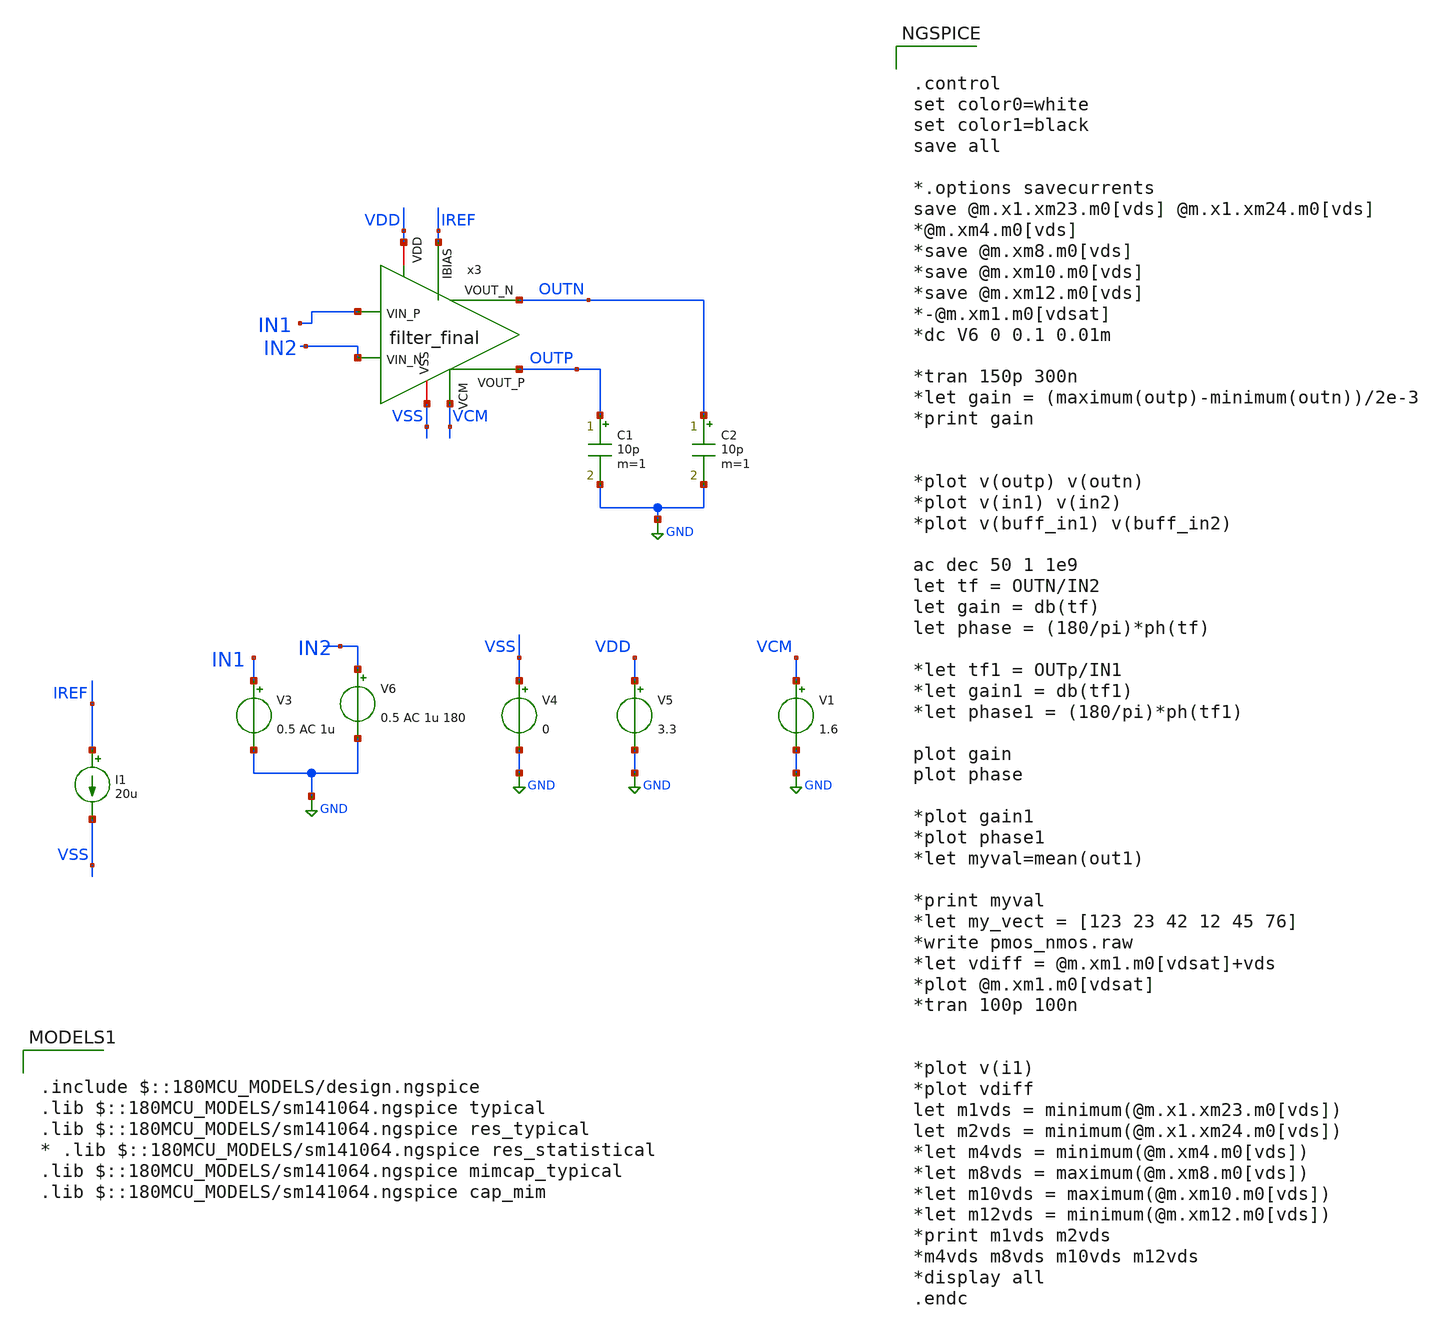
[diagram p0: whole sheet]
** sch_path: AWG_OUTPUT_AND_MUX_PAKISTAN_05/xschem/filter_test.sch
**.subckt filter_test
V3 IN1 GND 0.5 AC 1u
V4 VSS GND 0
V5 VDD GND 3.3
V6 IN2 GND 0.5 AC 1u 180
I1 IREF VSS 20u
C1 OUTP GND 10p m=1
C2 OUTN GND 10p m=1
V1 VCM GND 1.6
x3 IN2 IN1 OUTP OUTN VDD IREF VCM VSS filter_final
**** begin user architecture code


.control
set color0=white
set color1=black
save all

*.options savecurrents
save @m.x1.xm23.m0[vds] @m.x1.xm24.m0[vds]
*@m.xm4.m0[vds]
*save @m.xm8.m0[vds]
*save @m.xm10.m0[vds]
*save @m.xm12.m0[vds]
*-@m.xm1.m0[vdsat]
*dc V6 0 0.1 0.01m

*tran 150p 300n
*let gain = (maximum(outp)-minimum(outn))/2e-3
*print gain


*plot v(outp) v(outn)
*plot v(in1) v(in2)
*plot v(buff_in1) v(buff_in2)

ac dec 50 1 1e9
let tf = OUTN/IN2
let gain = db(tf)
let phase = (180/pi)*ph(tf)

*let tf1 = OUTp/IN1
*let gain1 = db(tf1)
*let phase1 = (180/pi)*ph(tf1)

plot gain
plot phase

*plot gain1
*plot phase1
*let myval=mean(out1)

*print myval
*let my_vect = [123 23 42 12 45 76]
*write pmos_nmos.raw
*let vdiff = @m.xm1.m0[vdsat]+vds
*plot @m.xm1.m0[vdsat]
*tran 100p 100n


*plot v(i1)
*plot vdiff
let m1vds = minimum(@m.x1.xm23.m0[vds])
let m2vds = minimum(@m.x1.xm24.m0[vds])
*let m4vds = minimum(@m.xm4.m0[vds])
*let m8vds = maximum(@m.xm8.m0[vds])
*let m10vds = maximum(@m.xm10.m0[vds])
*let m12vds = minimum(@m.xm12.m0[vds])
*print m1vds m2vds
*m4vds m8vds m10vds m12vds
*display all
.endc



.include $::180MCU_MODELS/design.ngspice
.lib $::180MCU_MODELS/sm141064.ngspice typical
.lib $::180MCU_MODELS/sm141064.ngspice res_typical
* .lib $::180MCU_MODELS/sm141064.ngspice res_statistical
.lib $::180MCU_MODELS/sm141064.ngspice mimcap_typical
.lib $::180MCU_MODELS/sm141064.ngspice cap_mim

**** end user architecture code
**.ends

* expanding   symbol:  filter_final.sym # of pins=8
** sym_path: AWG_OUTPUT_AND_MUX_PAKISTAN_05/xschem/filter_final.sym
** sch_path: AWG_OUTPUT_AND_MUX_PAKISTAN_05/xschem/filter_final.sch
.subckt filter_final VIN_N VIN_P VOUT_P VOUT_N VDD IBIAS VCM VSS
*.iopin VDD
*.iopin VSS
*.opin VOUT_N
*.opin VOUT_P
*.ipin VIN_N
*.ipin VIN_P
*.ipin IBIAS
*.ipin VCM
XR37 net7 VIN_P VDD ppolyf_u r_width=1e-6 r_length=2.3e-6 m=1
XR1 net1 VIN_N VDD ppolyf_u r_width=1e-6 r_length=2.3e-6 m=1
XR2 net8 net7 VDD ppolyf_u r_width=1e-6 r_length=2.3e-6 m=1
XR3 net2 net1 VDD ppolyf_u r_width=1e-6 r_length=2.3e-6 m=1
XR4 R7_R3_P net8 VDD ppolyf_u r_width=1e-6 r_length=2.3e-6 m=1
XR5 R7_R3_N net2 VDD ppolyf_u r_width=1e-6 r_length=2.3e-6 m=1
XR6 net9 R7_R3_P VDD ppolyf_u r_width=1e-6 r_length=2.3e-6 m=1
XR7 net3 R7_R3_N VDD ppolyf_u r_width=1e-6 r_length=2.3e-6 m=1
XR8 net10 net9 VDD ppolyf_u r_width=1e-6 r_length=2.3e-6 m=1
XR9 net4 net3 VDD ppolyf_u r_width=1e-6 r_length=2.3e-6 m=1
XR10 net12 net10 VDD ppolyf_u r_width=1e-6 r_length=2.3e-6 m=1
XR11 net50 net4 VDD ppolyf_u r_width=1e-6 r_length=2.3e-6 m=1
XR12 net11 net12 VDD ppolyf_u r_width=1e-6 r_length=2.3e-6 m=1
XR13 net5 net50 VDD ppolyf_u r_width=1e-6 r_length=2.3e-6 m=1
XR14 net13 net11 VDD ppolyf_u r_width=1e-6 r_length=2.3e-6 m=1
XR15 net6 net5 VDD ppolyf_u r_width=1e-6 r_length=2.3e-6 m=1
XR16 net14 net13 VDD ppolyf_u r_width=1e-6 r_length=2.3e-6 m=1
XR17 net15 net6 VDD ppolyf_u r_width=1e-6 r_length=2.3e-6 m=1
XR18 R7_R10_R8_P net14 VDD ppolyf_u r_width=1e-6 r_length=2.3e-6 m=1
XR19 R7_R10_R8_N net15 VDD ppolyf_u r_width=1e-6 r_length=2.3e-6 m=1
XR20 net20 R7_R10_R8_P VDD ppolyf_u r_width=1e-6 r_length=2.3e-6 m=1
XR21 net16 R7_R10_R8_N VDD ppolyf_u r_width=1e-6 r_length=2.3e-6 m=1
XR22 net21 net20 VDD ppolyf_u r_width=1e-6 r_length=2.3e-6 m=1
XR23 net17 net16 VDD ppolyf_u r_width=1e-6 r_length=2.3e-6 m=1
XR24 net23 net21 VDD ppolyf_u r_width=1e-6 r_length=2.3e-6 m=1
XR25 net49 net17 VDD ppolyf_u r_width=1e-6 r_length=2.3e-6 m=1
XR26 net22 net23 VDD ppolyf_u r_width=1e-6 r_length=2.3e-6 m=1
XR27 net18 net49 VDD ppolyf_u r_width=1e-6 r_length=2.3e-6 m=1
XR28 net24 net22 VDD ppolyf_u r_width=1e-6 r_length=2.3e-6 m=1
XR29 net19 net18 VDD ppolyf_u r_width=1e-6 r_length=2.3e-6 m=1
XR30 net25 net24 VDD ppolyf_u r_width=1e-6 r_length=2.3e-6 m=1
XR31 net26 net19 VDD ppolyf_u r_width=1e-6 r_length=2.3e-6 m=1
XR32 net27 net25 VDD ppolyf_u r_width=1e-6 r_length=2.3e-6 m=1
XR33 net28 net26 VDD ppolyf_u r_width=1e-6 r_length=2.3e-6 m=1
XR34 net46 net27 VDD ppolyf_u r_width=1e-6 r_length=2.3e-6 m=1
XR35 net47 net28 VDD ppolyf_u r_width=1e-6 r_length=2.3e-6 m=1
XR36 net29 R7_R10_R8_N VDD ppolyf_u r_width=1e-6 r_length=2.3e-6 m=1
XR38 net30 net29 VDD ppolyf_u r_width=1e-6 r_length=2.3e-6 m=1
XR39 net48 net30 VDD ppolyf_u r_width=1e-6 r_length=2.3e-6 m=1
XR40 net31 net48 VDD ppolyf_u r_width=1e-6 r_length=2.3e-6 m=1
XR41 net32 net31 VDD ppolyf_u r_width=1e-6 r_length=2.3e-6 m=1
XR42 net33 net32 VDD ppolyf_u r_width=1e-6 r_length=2.3e-6 m=1
XR43 net34 net33 VDD ppolyf_u r_width=1e-6 r_length=2.3e-6 m=1
XR44 net45 net34 VDD ppolyf_u r_width=1e-6 r_length=2.3e-6 m=1
XR45 net35 net42 VDD ppolyf_u r_width=1e-6 r_length=2.3e-6 m=1
XR46 net36 net35 VDD ppolyf_u r_width=1e-6 r_length=2.3e-6 m=1
XR47 net38 net36 VDD ppolyf_u r_width=1e-6 r_length=2.3e-6 m=1
XR48 net37 net38 VDD ppolyf_u r_width=1e-6 r_length=2.3e-6 m=1
XR49 net39 net37 VDD ppolyf_u r_width=1e-6 r_length=2.3e-6 m=1
XR50 net40 net39 VDD ppolyf_u r_width=1e-6 r_length=2.3e-6 m=1
XR51 net41 net40 VDD ppolyf_u r_width=1e-6 r_length=2.3e-6 m=1
XR52 R7_R10_R8_P net41 VDD ppolyf_u r_width=1e-6 r_length=2.3e-6 m=1
XR53 net43 VOUT_N VDD ppolyf_u r_width=1e-6 r_length=2.3e-6 m=1
XR54 net42 net43 VDD ppolyf_u r_width=1e-6 r_length=2.3e-6 m=1
XR55 net44 net45 VDD ppolyf_u r_width=1e-6 r_length=2.3e-6 m=1
XR56 VOUT_P net44 VDD ppolyf_u r_width=1e-6 r_length=2.3e-6 m=1
XR57 net46 net46 VDD ppolyf_u r_width=1e-6 r_length=2.3e-6 m=1
XR58 net47 net47 VDD ppolyf_u r_width=1e-6 r_length=2.3e-6 m=1
XR59 net46 net46 VDD ppolyf_u r_width=1e-6 r_length=2.3e-6 m=1
XR60 net47 net47 VDD ppolyf_u r_width=1e-6 r_length=2.3e-6 m=1
XC5 VOUT_N net46 cap_mim_2f0_m4m5_noshield c_width=16e-6 c_length=15.2e-6 m=1
XC6 VOUT_P net47 cap_mim_2f0_m4m5_noshield c_width=16e-6 c_length=15.2e-6 m=1
XR61 VDD VDD VDD ppolyf_u r_width=1e-6 r_length=2.3e-6 m=1
XR62 VDD VDD VDD ppolyf_u r_width=1e-6 r_length=2.3e-6 m=1
XR63 VDD VDD VDD ppolyf_u r_width=1e-6 r_length=2.3e-6 m=1
XR64 VDD VDD VDD ppolyf_u r_width=1e-6 r_length=2.3e-6 m=1
XR65 VDD VDD VDD ppolyf_u r_width=1e-6 r_length=2.3e-6 m=1
XR66 VDD VDD VDD ppolyf_u r_width=1e-6 r_length=2.3e-6 m=1
XR67 VDD VDD VDD ppolyf_u r_width=1e-6 r_length=2.3e-6 m=1
XR68 VDD VDD VDD ppolyf_u r_width=1e-6 r_length=2.3e-6 m=1
XR69 VDD VDD VDD ppolyf_u r_width=1e-6 r_length=2.3e-6 m=1
XR70 VDD VDD VDD ppolyf_u r_width=1e-6 r_length=2.3e-6 m=1
XR71 VDD VDD VDD ppolyf_u r_width=1e-6 r_length=2.3e-6 m=1
XR72 VDD VDD VDD ppolyf_u r_width=1e-6 r_length=2.3e-6 m=1
XC8 VOUT_P net47 cap_mim_2f0_m4m5_noshield c_width=16e-6 c_length=15.2e-6 m=1
XC9 VOUT_N net46 cap_mim_2f0_m4m5_noshield c_width=16e-6 c_length=15.2e-6 m=1
x1 VDD VSS net47 net46 IBIAS VCM VOUT_N VOUT_P Folded_Cascode_Diff
XC1 R7_R10_R8_N R7_R10_R8_P cap_mim_2f0_m4m5_noshield c_width=16e-6 c_length=15.2e-6 m=1
XC2 R7_R10_R8_N R7_R10_R8_P cap_mim_2f0_m4m5_noshield c_width=16e-6 c_length=15.2e-6 m=1
XC3 R7_R3_P R7_R3_N cap_mim_2f0_m4m5_noshield c_width=16e-6 c_length=15.2e-6 m=1
XC4 R7_R3_P R7_R3_N cap_mim_2f0_m4m5_noshield c_width=16e-6 c_length=15.2e-6 m=1
XC7 R7_R3_P R7_R3_N cap_mim_2f0_m4m5_noshield c_width=16e-6 c_length=15.2e-6 m=1
XC10 R7_R3_P R7_R3_N cap_mim_2f0_m4m5_noshield c_width=16e-6 c_length=15.2e-6 m=1
XC12 R7_R3_P R7_R3_N cap_mim_2f0_m4m5_noshield c_width=16e-6 c_length=15.2e-6 m=1
XC13 R7_R3_P R7_R3_N cap_mim_2f0_m4m5_noshield c_width=16e-6 c_length=15.2e-6 m=1
.ends


* expanding   symbol:  Folded_Cascode_Diff.sym # of pins=8
** sym_path: AWG_OUTPUT_AND_MUX_PAKISTAN_05/xschem/Folded_Cascode_Diff.sym
** sch_path: AWG_OUTPUT_AND_MUX_PAKISTAN_05/xschem/Folded_Cascode_Diff.sch
.subckt Folded_Cascode_Diff VDD VSS IN_N IN_P IBIAS1 VCM OUT_N OUT_P
*.iopin VDD
*.iopin VSS
*.iopin IN_N
*.iopin IN_P
*.iopin IBIAS1
*.iopin VCM
*.iopin OUT_N
*.iopin OUT_P
XM1 VPD VB1 VDD VDD pfet_03v3 L=0.28u W=50u nf=1 ad='int((nf+1)/2) * W/nf * 0.18u' as='int((nf+2)/2) * W/nf * 0.18u'
+ pd='2*int((nf+1)/2) * (W/nf + 0.18u)' ps='2*int((nf+2)/2) * (W/nf + 0.18u)' nrd='0.18u / W' nrs='0.18u / W'
+ sa=0 sb=0 sd=0 m=1
XM2 VND VB1 VDD VDD pfet_03v3 L=0.28u W=50u nf=1 ad='int((nf+1)/2) * W/nf * 0.18u' as='int((nf+2)/2) * W/nf * 0.18u'
+ pd='2*int((nf+1)/2) * (W/nf + 0.18u)' ps='2*int((nf+2)/2) * (W/nf + 0.18u)' nrd='0.18u / W' nrs='0.18u / W'
+ sa=0 sb=0 sd=0 m=1
XM3 OUT1 VB2 VND VDD pfet_03v3 L=0.28u W=50u nf=1 ad='int((nf+1)/2) * W/nf * 0.18u' as='int((nf+2)/2) * W/nf * 0.18u'
+ pd='2*int((nf+1)/2) * (W/nf + 0.18u)' ps='2*int((nf+2)/2) * (W/nf + 0.18u)' nrd='0.18u / W' nrs='0.18u / W'
+ sa=0 sb=0 sd=0 m=1
XM4 OUT2 VB2 VPD VDD pfet_03v3 L=0.28u W=50u nf=1 ad='int((nf+1)/2) * W/nf * 0.18u' as='int((nf+2)/2) * W/nf * 0.18u'
+ pd='2*int((nf+1)/2) * (W/nf + 0.18u)' ps='2*int((nf+2)/2) * (W/nf + 0.18u)' nrd='0.18u / W' nrs='0.18u / W'
+ sa=0 sb=0 sd=0 m=1
XM5 OUT2 VB3 IPD VSS nfet_03v3 L=0.28u W=46u nf=1 ad='int((nf+1)/2) * W/nf * 0.18u' as='int((nf+2)/2) * W/nf * 0.18u'
+ pd='2*int((nf+1)/2) * (W/nf + 0.18u)' ps='2*int((nf+2)/2) * (W/nf + 0.18u)' nrd='0.18u / W' nrs='0.18u / W'
+ sa=0 sb=0 sd=0 m=1
XM6 OUT1 VB3 IND VSS nfet_03v3 L=0.28u W=46u nf=1 ad='int((nf+1)/2) * W/nf * 0.18u' as='int((nf+2)/2) * W/nf * 0.18u'
+ pd='2*int((nf+1)/2) * (W/nf + 0.18u)' ps='2*int((nf+2)/2) * (W/nf + 0.18u)' nrd='0.18u / W' nrs='0.18u / W'
+ sa=0 sb=0 sd=0 m=1
XM7 IPD VB4 VSS VSS nfet_03v3 L=0.28u W=92u nf=1 ad='int((nf+1)/2) * W/nf * 0.18u' as='int((nf+2)/2) * W/nf * 0.18u'
+ pd='2*int((nf+1)/2) * (W/nf + 0.18u)' ps='2*int((nf+2)/2) * (W/nf + 0.18u)' nrd='0.18u / W' nrs='0.18u / W'
+ sa=0 sb=0 sd=0 m=1
XM8 IND VB4 VSS VSS nfet_03v3 L=0.28u W=92u nf=1 ad='int((nf+1)/2) * W/nf * 0.18u' as='int((nf+2)/2) * W/nf * 0.18u'
+ pd='2*int((nf+1)/2) * (W/nf + 0.18u)' ps='2*int((nf+2)/2) * (W/nf + 0.18u)' nrd='0.18u / W' nrs='0.18u / W'
+ sa=0 sb=0 sd=0 m=1
XM9 BD IBIAS VDD VDD pfet_03v3 L=0.56u W=100u nf=1 ad='int((nf+1)/2) * W/nf * 0.18u' as='int((nf+2)/2) * W/nf * 0.18u'
+ pd='2*int((nf+1)/2) * (W/nf + 0.18u)' ps='2*int((nf+2)/2) * (W/nf + 0.18u)' nrd='0.18u / W' nrs='0.18u / W'
+ sa=0 sb=0 sd=0 m=1
XM10 IPD IN_P BD VDD pfet_03v3 L=0.28u W=90u nf=1 ad='int((nf+1)/2) * W/nf * 0.18u' as='int((nf+2)/2) * W/nf * 0.18u'
+ pd='2*int((nf+1)/2) * (W/nf + 0.18u)' ps='2*int((nf+2)/2) * (W/nf + 0.18u)' nrd='0.18u / W' nrs='0.18u / W'
+ sa=0 sb=0 sd=0 m=1
XM11 IND IN_N BD VDD pfet_03v3 L=0.28u W=90u nf=1 ad='int((nf+1)/2) * W/nf * 0.18u' as='int((nf+2)/2) * W/nf * 0.18u'
+ pd='2*int((nf+1)/2) * (W/nf + 0.18u)' ps='2*int((nf+2)/2) * (W/nf + 0.18u)' nrd='0.18u / W' nrs='0.18u / W'
+ sa=0 sb=0 sd=0 m=1
XM53 VDD VDD VDD VDD pfet_03v3 L=0.56u W=25.04u nf=1 ad='int((nf+1)/2) * W/nf * 0.18u' as='int((nf+2)/2) * W/nf * 0.18u'
+ pd='2*int((nf+1)/2) * (W/nf + 0.18u)' ps='2*int((nf+2)/2) * (W/nf + 0.18u)' nrd='0.18u / W' nrs='0.18u / W'
+ sa=0 sb=0 sd=0 m=1
XM13 IBS IBIAS1 VDD VDD pfet_03v3 L=0.56u W=20u nf=1 ad='int((nf+1)/2) * W/nf * 0.18u' as='int((nf+2)/2) * W/nf * 0.18u'
+ pd='2*int((nf+1)/2) * (W/nf + 0.18u)' ps='2*int((nf+2)/2) * (W/nf + 0.18u)' nrd='0.18u / W' nrs='0.18u / W'
+ sa=0 sb=0 sd=0 m=1
XM14 IBS IBS VSS VSS nfet_03v3 L=1u W=2u nf=1 ad='int((nf+1)/2) * W/nf * 0.18u' as='int((nf+2)/2) * W/nf * 0.18u'
+ pd='2*int((nf+1)/2) * (W/nf + 0.18u)' ps='2*int((nf+2)/2) * (W/nf + 0.18u)' nrd='0.18u / W' nrs='0.18u / W'
+ sa=0 sb=0 sd=0 m=1
XM15 IBIAS IBS VSS VSS nfet_03v3 L=1u W=2u nf=1 ad='int((nf+1)/2) * W/nf * 0.18u' as='int((nf+2)/2) * W/nf * 0.18u'
+ pd='2*int((nf+1)/2) * (W/nf + 0.18u)' ps='2*int((nf+2)/2) * (W/nf + 0.18u)' nrd='0.18u / W' nrs='0.18u / W'
+ sa=0 sb=0 sd=0 m=1
XM16 IBIAS IBIAS VDD VDD pfet_03v3 L=0.56u W=20u nf=1 ad='int((nf+1)/2) * W/nf * 0.18u' as='int((nf+2)/2) * W/nf * 0.18u'
+ pd='2*int((nf+1)/2) * (W/nf + 0.18u)' ps='2*int((nf+2)/2) * (W/nf + 0.18u)' nrd='0.18u / W' nrs='0.18u / W'
+ sa=0 sb=0 sd=0 m=1
XM17 IBIAS1 IBIAS1 VDD VDD pfet_03v3 L=0.56u W=4u nf=1 ad='int((nf+1)/2) * W/nf * 0.18u' as='int((nf+2)/2) * W/nf * 0.18u'
+ pd='2*int((nf+1)/2) * (W/nf + 0.18u)' ps='2*int((nf+2)/2) * (W/nf + 0.18u)' nrd='0.18u / W' nrs='0.18u / W'
+ sa=0 sb=0 sd=0 m=1
XM19 VBIASN IBIAS1 VDD VDD pfet_03v3 L=0.56u W=4u nf=1 ad='int((nf+1)/2) * W/nf * 0.18u' as='int((nf+2)/2) * W/nf * 0.18u'
+ pd='2*int((nf+1)/2) * (W/nf + 0.18u)' ps='2*int((nf+2)/2) * (W/nf + 0.18u)' nrd='0.18u / W' nrs='0.18u / W'
+ sa=0 sb=0 sd=0 m=1
XM20 VBIASN VBIASN VSS VSS nfet_03v3 L=0.56u W=2u nf=1 ad='int((nf+1)/2) * W/nf * 0.18u' as='int((nf+2)/2) * W/nf * 0.18u'
+ pd='2*int((nf+1)/2) * (W/nf + 0.18u)' ps='2*int((nf+2)/2) * (W/nf + 0.18u)' nrd='0.18u / W' nrs='0.18u / W'
+ sa=0 sb=0 sd=0 m=1
XM26 IB2 VB2 VDD VDD pfet_03v3 L=1u W=0.5u nf=1 ad='int((nf+1)/2) * W/nf * 0.18u' as='int((nf+2)/2) * W/nf * 0.18u'
+ pd='2*int((nf+1)/2) * (W/nf + 0.18u)' ps='2*int((nf+2)/2) * (W/nf + 0.18u)' nrd='0.18u / W' nrs='0.18u / W'
+ sa=0 sb=0 sd=0 m=1
XM27 VB2 VB2 IB2 VDD pfet_03v3 L=0.28u W=8u nf=1 ad='int((nf+1)/2) * W/nf * 0.18u' as='int((nf+2)/2) * W/nf * 0.18u'
+ pd='2*int((nf+1)/2) * (W/nf + 0.18u)' ps='2*int((nf+2)/2) * (W/nf + 0.18u)' nrd='0.18u / W' nrs='0.18u / W'
+ sa=0 sb=0 sd=0 m=1
XM28 VB2 VBIASN VSS VSS nfet_03v3 L=0.56u W=1u nf=1 ad='int((nf+1)/2) * W/nf * 0.18u' as='int((nf+2)/2) * W/nf * 0.18u'
+ pd='2*int((nf+1)/2) * (W/nf + 0.18u)' ps='2*int((nf+2)/2) * (W/nf + 0.18u)' nrd='0.18u / W' nrs='0.18u / W'
+ sa=0 sb=0 sd=0 m=1
XM21 VCD VBIASN VSS VSS nfet_03v3 L=0.56u W=6u nf=1 ad='int((nf+1)/2) * W/nf * 0.18u' as='int((nf+2)/2) * W/nf * 0.18u'
+ pd='2*int((nf+1)/2) * (W/nf + 0.18u)' ps='2*int((nf+2)/2) * (W/nf + 0.18u)' nrd='0.18u / W' nrs='0.18u / W'
+ sa=0 sb=0 sd=0 m=1
XM22 VBM VCM VCD VSS nfet_03v3 L=0.28u W=30u nf=1 ad='int((nf+1)/2) * W/nf * 0.18u' as='int((nf+2)/2) * W/nf * 0.18u'
+ pd='2*int((nf+1)/2) * (W/nf + 0.18u)' ps='2*int((nf+2)/2) * (W/nf + 0.18u)' nrd='0.18u / W' nrs='0.18u / W'
+ sa=0 sb=0 sd=0 m=1
XM23 VB1 VOUT VCD VSS nfet_03v3 L=0.28u W=30u nf=1 ad='int((nf+1)/2) * W/nf * 0.18u' as='int((nf+2)/2) * W/nf * 0.18u'
+ pd='2*int((nf+1)/2) * (W/nf + 0.18u)' ps='2*int((nf+2)/2) * (W/nf + 0.18u)' nrd='0.18u / W' nrs='0.18u / W'
+ sa=0 sb=0 sd=0 m=1
XM24 VBM VBM VDD VDD pfet_03v3 L=0.28u W=8u nf=1 ad='int((nf+1)/2) * W/nf * 0.18u' as='int((nf+2)/2) * W/nf * 0.18u'
+ pd='2*int((nf+1)/2) * (W/nf + 0.18u)' ps='2*int((nf+2)/2) * (W/nf + 0.18u)' nrd='0.18u / W' nrs='0.18u / W'
+ sa=0 sb=0 sd=0 m=1
XM25 VB1 VB1 VDD VDD pfet_03v3 L=0.28u W=8u nf=1 ad='int((nf+1)/2) * W/nf * 0.18u' as='int((nf+2)/2) * W/nf * 0.18u'
+ pd='2*int((nf+1)/2) * (W/nf + 0.18u)' ps='2*int((nf+2)/2) * (W/nf + 0.18u)' nrd='0.18u / W' nrs='0.18u / W'
+ sa=0 sb=0 sd=0 m=1
XM18 IB5 IBIAS1 VDD VDD pfet_03v3 L=0.56u W=16u nf=1 ad='int((nf+1)/2) * W/nf * 0.18u' as='int((nf+2)/2) * W/nf * 0.18u'
+ pd='2*int((nf+1)/2) * (W/nf + 0.18u)' ps='2*int((nf+2)/2) * (W/nf + 0.18u)' nrd='0.18u / W' nrs='0.18u / W'
+ sa=0 sb=0 sd=0 m=1
XM29 IB5 IB5 VB4 VSS nfet_03v3 L=0.28u W=4u nf=1 ad='int((nf+1)/2) * W/nf * 0.18u' as='int((nf+2)/2) * W/nf * 0.18u'
+ pd='2*int((nf+1)/2) * (W/nf + 0.18u)' ps='2*int((nf+2)/2) * (W/nf + 0.18u)' nrd='0.18u / W' nrs='0.18u / W'
+ sa=0 sb=0 sd=0 m=1
XM30 VB4 VB4 VSS VSS nfet_03v3 L=0.28u W=14u nf=1 ad='int((nf+1)/2) * W/nf * 0.18u' as='int((nf+2)/2) * W/nf * 0.18u'
+ pd='2*int((nf+1)/2) * (W/nf + 0.18u)' ps='2*int((nf+2)/2) * (W/nf + 0.18u)' nrd='0.18u / W' nrs='0.18u / W'
+ sa=0 sb=0 sd=0 m=1
XM32 VB3 IBIAS1 VDD VDD pfet_03v3 L=0.56u W=8u nf=1 ad='int((nf+1)/2) * W/nf * 0.18u' as='int((nf+2)/2) * W/nf * 0.18u'
+ pd='2*int((nf+1)/2) * (W/nf + 0.18u)' ps='2*int((nf+2)/2) * (W/nf + 0.18u)' nrd='0.18u / W' nrs='0.18u / W'
+ sa=0 sb=0 sd=0 m=1
XM33 VB3 VB3 IB3 VSS nfet_03v3 L=0.28u W=7u nf=1 ad='int((nf+1)/2) * W/nf * 0.18u' as='int((nf+2)/2) * W/nf * 0.18u'
+ pd='2*int((nf+1)/2) * (W/nf + 0.18u)' ps='2*int((nf+2)/2) * (W/nf + 0.18u)' nrd='0.18u / W' nrs='0.18u / W'
+ sa=0 sb=0 sd=0 m=1
XM34 IB3 VB3 VSS VSS nfet_03v3 L=0.56u W=1u nf=1 ad='int((nf+1)/2) * W/nf * 0.18u' as='int((nf+2)/2) * W/nf * 0.18u'
+ pd='2*int((nf+1)/2) * (W/nf + 0.18u)' ps='2*int((nf+2)/2) * (W/nf + 0.18u)' nrd='0.18u / W' nrs='0.18u / W'
+ sa=0 sb=0 sd=0 m=1
XM36 OUT_P IBIAS2 VDD VDD pfet_03v3 L=0.28u W=84u nf=1 ad='int((nf+1)/2) * W/nf * 0.18u' as='int((nf+2)/2) * W/nf * 0.18u'
+ pd='2*int((nf+1)/2) * (W/nf + 0.18u)' ps='2*int((nf+2)/2) * (W/nf + 0.18u)' nrd='0.18u / W' nrs='0.18u / W'
+ sa=0 sb=0 sd=0 m=1
XM38 OUT_P OUT2 VSS VSS nfet_03v3 L=0.28u W=72u nf=1 ad='int((nf+1)/2) * W/nf * 0.18u' as='int((nf+2)/2) * W/nf * 0.18u'
+ pd='2*int((nf+1)/2) * (W/nf + 0.18u)' ps='2*int((nf+2)/2) * (W/nf + 0.18u)' nrd='0.18u / W' nrs='0.18u / W'
+ sa=0 sb=0 sd=0 m=1
XM39 OUT_P IBIAS2 VDD VDD pfet_03v3 L=0.28u W=84u nf=1 ad='int((nf+1)/2) * W/nf * 0.18u' as='int((nf+2)/2) * W/nf * 0.18u'
+ pd='2*int((nf+1)/2) * (W/nf + 0.18u)' ps='2*int((nf+2)/2) * (W/nf + 0.18u)' nrd='0.18u / W' nrs='0.18u / W'
+ sa=0 sb=0 sd=0 m=1
XM40 OUT_N IBIAS2 VDD VDD pfet_03v3 L=0.28u W=84u nf=1 ad='int((nf+1)/2) * W/nf * 0.18u' as='int((nf+2)/2) * W/nf * 0.18u'
+ pd='2*int((nf+1)/2) * (W/nf + 0.18u)' ps='2*int((nf+2)/2) * (W/nf + 0.18u)' nrd='0.18u / W' nrs='0.18u / W'
+ sa=0 sb=0 sd=0 m=1
XM41 OUT_N OUT1 VSS VSS nfet_03v3 L=0.28u W=72u nf=1 ad='int((nf+1)/2) * W/nf * 0.18u' as='int((nf+2)/2) * W/nf * 0.18u'
+ pd='2*int((nf+1)/2) * (W/nf + 0.18u)' ps='2*int((nf+2)/2) * (W/nf + 0.18u)' nrd='0.18u / W' nrs='0.18u / W'
+ sa=0 sb=0 sd=0 m=1
XM42 OUT_N IBIAS2 VDD VDD pfet_03v3 L=0.28u W=84u nf=1 ad='int((nf+1)/2) * W/nf * 0.18u' as='int((nf+2)/2) * W/nf * 0.18u'
+ pd='2*int((nf+1)/2) * (W/nf + 0.18u)' ps='2*int((nf+2)/2) * (W/nf + 0.18u)' nrd='0.18u / W' nrs='0.18u / W'
+ sa=0 sb=0 sd=0 m=1
XM43 OUT_N OUT1 VSS VSS nfet_03v3 L=0.28u W=72u nf=1 ad='int((nf+1)/2) * W/nf * 0.18u' as='int((nf+2)/2) * W/nf * 0.18u'
+ pd='2*int((nf+1)/2) * (W/nf + 0.18u)' ps='2*int((nf+2)/2) * (W/nf + 0.18u)' nrd='0.18u / W' nrs='0.18u / W'
+ sa=0 sb=0 sd=0 m=1
XM44 OUT_P OUT2 VSS VSS nfet_03v3 L=0.28u W=72u nf=1 ad='int((nf+1)/2) * W/nf * 0.18u' as='int((nf+2)/2) * W/nf * 0.18u'
+ pd='2*int((nf+1)/2) * (W/nf + 0.18u)' ps='2*int((nf+2)/2) * (W/nf + 0.18u)' nrd='0.18u / W' nrs='0.18u / W'
+ sa=0 sb=0 sd=0 m=1
XM45 OUT_N IBIAS2 VDD VDD pfet_03v3 L=0.28u W=84u nf=1 ad='int((nf+1)/2) * W/nf * 0.18u' as='int((nf+2)/2) * W/nf * 0.18u'
+ pd='2*int((nf+1)/2) * (W/nf + 0.18u)' ps='2*int((nf+2)/2) * (W/nf + 0.18u)' nrd='0.18u / W' nrs='0.18u / W'
+ sa=0 sb=0 sd=0 m=1
XM46 OUT_P IBIAS2 VDD VDD pfet_03v3 L=0.28u W=84u nf=1 ad='int((nf+1)/2) * W/nf * 0.18u' as='int((nf+2)/2) * W/nf * 0.18u'
+ pd='2*int((nf+1)/2) * (W/nf + 0.18u)' ps='2*int((nf+2)/2) * (W/nf + 0.18u)' nrd='0.18u / W' nrs='0.18u / W'
+ sa=0 sb=0 sd=0 m=1
XM47 OUT_P IBIAS2 VDD VDD pfet_03v3 L=0.28u W=84u nf=1 ad='int((nf+1)/2) * W/nf * 0.18u' as='int((nf+2)/2) * W/nf * 0.18u'
+ pd='2*int((nf+1)/2) * (W/nf + 0.18u)' ps='2*int((nf+2)/2) * (W/nf + 0.18u)' nrd='0.18u / W' nrs='0.18u / W'
+ sa=0 sb=0 sd=0 m=1
XM48 OUT_N IBIAS2 VDD VDD pfet_03v3 L=0.28u W=84u nf=1 ad='int((nf+1)/2) * W/nf * 0.18u' as='int((nf+2)/2) * W/nf * 0.18u'
+ pd='2*int((nf+1)/2) * (W/nf + 0.18u)' ps='2*int((nf+2)/2) * (W/nf + 0.18u)' nrd='0.18u / W' nrs='0.18u / W'
+ sa=0 sb=0 sd=0 m=1
XM50 OUT_N OUT1 VSS VSS nfet_03v3 L=0.28u W=72u nf=1 ad='int((nf+1)/2) * W/nf * 0.18u' as='int((nf+2)/2) * W/nf * 0.18u'
+ pd='2*int((nf+1)/2) * (W/nf + 0.18u)' ps='2*int((nf+2)/2) * (W/nf + 0.18u)' nrd='0.18u / W' nrs='0.18u / W'
+ sa=0 sb=0 sd=0 m=1
XM51 OUT_P OUT2 VSS VSS nfet_03v3 L=0.28u W=72u nf=1 ad='int((nf+1)/2) * W/nf * 0.18u' as='int((nf+2)/2) * W/nf * 0.18u'
+ pd='2*int((nf+1)/2) * (W/nf + 0.18u)' ps='2*int((nf+2)/2) * (W/nf + 0.18u)' nrd='0.18u / W' nrs='0.18u / W'
+ sa=0 sb=0 sd=0 m=1
XM52 OUT_P IBIAS2 VDD VDD pfet_03v3 L=0.28u W=84u nf=1 ad='int((nf+1)/2) * W/nf * 0.18u' as='int((nf+2)/2) * W/nf * 0.18u'
+ pd='2*int((nf+1)/2) * (W/nf + 0.18u)' ps='2*int((nf+2)/2) * (W/nf + 0.18u)' nrd='0.18u / W' nrs='0.18u / W'
+ sa=0 sb=0 sd=0 m=1
XM54 OUT_N IBIAS2 VDD VDD pfet_03v3 L=0.28u W=84u nf=1 ad='int((nf+1)/2) * W/nf * 0.18u' as='int((nf+2)/2) * W/nf * 0.18u'
+ pd='2*int((nf+1)/2) * (W/nf + 0.18u)' ps='2*int((nf+2)/2) * (W/nf + 0.18u)' nrd='0.18u / W' nrs='0.18u / W'
+ sa=0 sb=0 sd=0 m=1
XM55 OUT_N IBIAS2 VDD VDD pfet_03v3 L=0.28u W=84u nf=1 ad='int((nf+1)/2) * W/nf * 0.18u' as='int((nf+2)/2) * W/nf * 0.18u'
+ pd='2*int((nf+1)/2) * (W/nf + 0.18u)' ps='2*int((nf+2)/2) * (W/nf + 0.18u)' nrd='0.18u / W' nrs='0.18u / W'
+ sa=0 sb=0 sd=0 m=1
XM57 OUT_P IBIAS2 VDD VDD pfet_03v3 L=0.28u W=84u nf=1 ad='int((nf+1)/2) * W/nf * 0.18u' as='int((nf+2)/2) * W/nf * 0.18u'
+ pd='2*int((nf+1)/2) * (W/nf + 0.18u)' ps='2*int((nf+2)/2) * (W/nf + 0.18u)' nrd='0.18u / W' nrs='0.18u / W'
+ sa=0 sb=0 sd=0 m=1
XM68 IBIAS2 IBIAS2 VDD VDD pfet_03v3 L=0.28u W=84u nf=1 ad='int((nf+1)/2) * W/nf * 0.18u' as='int((nf+2)/2) * W/nf * 0.18u'
+ pd='2*int((nf+1)/2) * (W/nf + 0.18u)' ps='2*int((nf+2)/2) * (W/nf + 0.18u)' nrd='0.18u / W' nrs='0.18u / W'
+ sa=0 sb=0 sd=0 m=1
XM69 IBIAS2 IBIAS2 VDD VDD pfet_03v3 L=0.28u W=84u nf=1 ad='int((nf+1)/2) * W/nf * 0.18u' as='int((nf+2)/2) * W/nf * 0.18u'
+ pd='2*int((nf+1)/2) * (W/nf + 0.18u)' ps='2*int((nf+2)/2) * (W/nf + 0.18u)' nrd='0.18u / W' nrs='0.18u / W'
+ sa=0 sb=0 sd=0 m=1
XM70 IVS IBIAS3 VDD VDD pfet_03v3 L=0.28u W=84u nf=1 ad='int((nf+1)/2) * W/nf * 0.18u' as='int((nf+2)/2) * W/nf * 0.18u'
+ pd='2*int((nf+1)/2) * (W/nf + 0.18u)' ps='2*int((nf+2)/2) * (W/nf + 0.18u)' nrd='0.18u / W' nrs='0.18u / W'
+ sa=0 sb=0 sd=0 m=1
XM71 IVS IVS VSS VSS nfet_03v3 L=1u W=20u nf=1 ad='int((nf+1)/2) * W/nf * 0.18u' as='int((nf+2)/2) * W/nf * 0.18u'
+ pd='2*int((nf+1)/2) * (W/nf + 0.18u)' ps='2*int((nf+2)/2) * (W/nf + 0.18u)' nrd='0.18u / W' nrs='0.18u / W'
+ sa=0 sb=0 sd=0 m=1
XM72 IBIAS2 IVS VSS VSS nfet_03v3 L=1u W=20u nf=1 ad='int((nf+1)/2) * W/nf * 0.18u' as='int((nf+2)/2) * W/nf * 0.18u'
+ pd='2*int((nf+1)/2) * (W/nf + 0.18u)' ps='2*int((nf+2)/2) * (W/nf + 0.18u)' nrd='0.18u / W' nrs='0.18u / W'
+ sa=0 sb=0 sd=0 m=1
XM73 IVS IBIAS3 VDD VDD pfet_03v3 L=0.28u W=84u nf=1 ad='int((nf+1)/2) * W/nf * 0.18u' as='int((nf+2)/2) * W/nf * 0.18u'
+ pd='2*int((nf+1)/2) * (W/nf + 0.18u)' ps='2*int((nf+2)/2) * (W/nf + 0.18u)' nrd='0.18u / W' nrs='0.18u / W'
+ sa=0 sb=0 sd=0 m=1
XM76 IBIAS3 IBIAS3 VDD VDD pfet_03v3 L=0.28u W=24u nf=1 ad='int((nf+1)/2) * W/nf * 0.18u' as='int((nf+2)/2) * W/nf * 0.18u'
+ pd='2*int((nf+1)/2) * (W/nf + 0.18u)' ps='2*int((nf+2)/2) * (W/nf + 0.18u)' nrd='0.18u / W' nrs='0.18u / W'
+ sa=0 sb=0 sd=0 m=1
XM77 IB4 IBIAS4 VDD VDD pfet_03v3 L=0.28u W=24u nf=1 ad='int((nf+1)/2) * W/nf * 0.18u' as='int((nf+2)/2) * W/nf * 0.18u'
+ pd='2*int((nf+1)/2) * (W/nf + 0.18u)' ps='2*int((nf+2)/2) * (W/nf + 0.18u)' nrd='0.18u / W' nrs='0.18u / W'
+ sa=0 sb=0 sd=0 m=1
XM78 IB4 IB4 VSS VSS nfet_03v3 L=1u W=10u nf=1 ad='int((nf+1)/2) * W/nf * 0.18u' as='int((nf+2)/2) * W/nf * 0.18u'
+ pd='2*int((nf+1)/2) * (W/nf + 0.18u)' ps='2*int((nf+2)/2) * (W/nf + 0.18u)' nrd='0.18u / W' nrs='0.18u / W'
+ sa=0 sb=0 sd=0 m=1
XM79 IBIAS3 IB4 VSS VSS nfet_03v3 L=1u W=10u nf=1 ad='int((nf+1)/2) * W/nf * 0.18u' as='int((nf+2)/2) * W/nf * 0.18u'
+ pd='2*int((nf+1)/2) * (W/nf + 0.18u)' ps='2*int((nf+2)/2) * (W/nf + 0.18u)' nrd='0.18u / W' nrs='0.18u / W'
+ sa=0 sb=0 sd=0 m=1
XM80 IBIAS4 IBIAS4 VDD VDD pfet_03v3 L=0.28u W=5u nf=1 ad='int((nf+1)/2) * W/nf * 0.18u' as='int((nf+2)/2) * W/nf * 0.18u'
+ pd='2*int((nf+1)/2) * (W/nf + 0.18u)' ps='2*int((nf+2)/2) * (W/nf + 0.18u)' nrd='0.18u / W' nrs='0.18u / W'
+ sa=0 sb=0 sd=0 m=1
XM81 IBIAS4 VBIASN VSS VSS nfet_03v3 L=1u W=2u nf=1 ad='int((nf+1)/2) * W/nf * 0.18u' as='int((nf+2)/2) * W/nf * 0.18u'
+ pd='2*int((nf+1)/2) * (W/nf + 0.18u)' ps='2*int((nf+2)/2) * (W/nf + 0.18u)' nrd='0.18u / W' nrs='0.18u / W'
+ sa=0 sb=0 sd=0 m=1
XR21 VDD VDD VDD ppolyf_u r_width=4e-6 r_length=6.2e-6 m=1
XR1 net2 OUT_P VDD ppolyf_u r_width=1e-6 r_length=5e-6 m=1
XR2 net2 net1 VDD ppolyf_u r_width=1e-6 r_length=5e-6 m=1
XR3 net3 net1 VDD ppolyf_u r_width=1e-6 r_length=5e-6 m=1
XR4 net3 net4 VDD ppolyf_u r_width=1e-6 r_length=5e-6 m=1
XR5 net5 net4 VDD ppolyf_u r_width=1e-6 r_length=5e-6 m=1
XR6 net5 net6 VDD ppolyf_u r_width=1e-6 r_length=5e-6 m=1
XR7 net7 net6 VDD ppolyf_u r_width=1e-6 r_length=5e-6 m=1
XR8 net7 net8 VDD ppolyf_u r_width=1e-6 r_length=5e-6 m=1
XR9 net9 net8 VDD ppolyf_u r_width=1e-6 r_length=5e-6 m=1
XR10 net9 VOUT VDD ppolyf_u r_width=1e-6 r_length=5e-6 m=1
XR11 net11 OUT_N VDD ppolyf_u r_width=1e-6 r_length=5e-6 m=1
XR12 net11 net10 VDD ppolyf_u r_width=1e-6 r_length=5e-6 m=1
XR13 net12 net10 VDD ppolyf_u r_width=1e-6 r_length=5e-6 m=1
XR14 net12 net13 VDD ppolyf_u r_width=1e-6 r_length=5e-6 m=1
XR15 net14 net13 VDD ppolyf_u r_width=1e-6 r_length=5e-6 m=1
XR16 net14 net15 VDD ppolyf_u r_width=1e-6 r_length=5e-6 m=1
XR17 net16 net15 VDD ppolyf_u r_width=1e-6 r_length=5e-6 m=1
XR18 net16 net17 VDD ppolyf_u r_width=1e-6 r_length=5e-6 m=1
XR19 net18 net17 VDD ppolyf_u r_width=1e-6 r_length=5e-6 m=1
XR20 net18 VOUT VDD ppolyf_u r_width=1e-6 r_length=5e-6 m=1
XR22 VOUT1 OUT1 VDD ppolyf_u r_width=1e-6 r_length=6.2e-6 m=1
XR23 VOUT2 OUT2 VDD ppolyf_u r_width=1e-6 r_length=6.2e-6 m=1
XR24 VOUT1 OUT1 VDD ppolyf_u r_width=1e-6 r_length=6.2e-6 m=1
XR25 VOUT2 OUT2 VDD ppolyf_u r_width=1e-6 r_length=6.2e-6 m=1
XR26 VOUT1 OUT1 VDD ppolyf_u r_width=1e-6 r_length=6.2e-6 m=1
XR27 VOUT2 OUT2 VDD ppolyf_u r_width=1e-6 r_length=6.2e-6 m=1
XR28 VOUT1 OUT1 VDD ppolyf_u r_width=1e-6 r_length=6.2e-6 m=1
XR29 VOUT2 OUT2 VDD ppolyf_u r_width=1e-6 r_length=6.2e-6 m=1
XR30 VDD VDD VDD ppolyf_u r_width=4e-6 r_length=5e-6 m=1
XC1 VOUT1 OUT_N cap_mim_2f0_m4m5_noshield c_width=21e-6 c_length=21e-6 m=1
XC2 VOUT2 OUT_P cap_mim_2f0_m4m5_noshield c_width=21e-6 c_length=21e-6 m=1
XC4 VOUT1 OUT_N cap_mim_2f0_m4m5_noshield c_width=21e-6 c_length=21e-6 m=1
XC5 VOUT2 OUT_P cap_mim_2f0_m4m5_noshield c_width=21e-6 c_length=21e-6 m=1
XM82 OUT_N IBIAS2 VDD VDD pfet_03v3 L=0.28u W=84u nf=1 ad='int((nf+1)/2) * W/nf * 0.18u' as='int((nf+2)/2) * W/nf * 0.18u'
+ pd='2*int((nf+1)/2) * (W/nf + 0.18u)' ps='2*int((nf+2)/2) * (W/nf + 0.18u)' nrd='0.18u / W' nrs='0.18u / W'
+ sa=0 sb=0 sd=0 m=1
XM83 OUT_P IBIAS2 VDD VDD pfet_03v3 L=0.28u W=84u nf=1 ad='int((nf+1)/2) * W/nf * 0.18u' as='int((nf+2)/2) * W/nf * 0.18u'
+ pd='2*int((nf+1)/2) * (W/nf + 0.18u)' ps='2*int((nf+2)/2) * (W/nf + 0.18u)' nrd='0.18u / W' nrs='0.18u / W'
+ sa=0 sb=0 sd=0 m=1
XM12 VDD VDD VDD VDD pfet_03v3 L=0.28u W=45u nf=1 ad='int((nf+1)/2) * W/nf * 0.18u' as='int((nf+2)/2) * W/nf * 0.18u'
+ pd='2*int((nf+1)/2) * (W/nf + 0.18u)' ps='2*int((nf+2)/2) * (W/nf + 0.18u)' nrd='0.18u / W' nrs='0.18u / W'
+ sa=0 sb=0 sd=0 m=1
XM31 VDD VDD VDD VDD pfet_03v3 L=0.28u W=25.04u nf=1 ad='int((nf+1)/2) * W/nf * 0.18u' as='int((nf+2)/2) * W/nf * 0.18u'
+ pd='2*int((nf+1)/2) * (W/nf + 0.18u)' ps='2*int((nf+2)/2) * (W/nf + 0.18u)' nrd='0.18u / W' nrs='0.18u / W'
+ sa=0 sb=0 sd=0 m=1
XM35 VDD VDD VDD VDD pfet_03v3 L=0.28u W=25.04u nf=1 ad='int((nf+1)/2) * W/nf * 0.18u' as='int((nf+2)/2) * W/nf * 0.18u'
+ pd='2*int((nf+1)/2) * (W/nf + 0.18u)' ps='2*int((nf+2)/2) * (W/nf + 0.18u)' nrd='0.18u / W' nrs='0.18u / W'
+ sa=0 sb=0 sd=0 m=1
XM37 VDD VDD VDD VDD pfet_03v3 L=0.28u W=24u nf=1 ad='int((nf+1)/2) * W/nf * 0.18u' as='int((nf+2)/2) * W/nf * 0.18u'
+ pd='2*int((nf+1)/2) * (W/nf + 0.18u)' ps='2*int((nf+2)/2) * (W/nf + 0.18u)' nrd='0.18u / W' nrs='0.18u / W'
+ sa=0 sb=0 sd=0 m=1
XM49 VDD VDD VDD VDD pfet_03v3 L=0.28u W=24u nf=1 ad='int((nf+1)/2) * W/nf * 0.18u' as='int((nf+2)/2) * W/nf * 0.18u'
+ pd='2*int((nf+1)/2) * (W/nf + 0.18u)' ps='2*int((nf+2)/2) * (W/nf + 0.18u)' nrd='0.18u / W' nrs='0.18u / W'
+ sa=0 sb=0 sd=0 m=1
XM56 VDD VDD VDD VDD pfet_03v3 L=0.28u W=24u nf=1 ad='int((nf+1)/2) * W/nf * 0.18u' as='int((nf+2)/2) * W/nf * 0.18u'
+ pd='2*int((nf+1)/2) * (W/nf + 0.18u)' ps='2*int((nf+2)/2) * (W/nf + 0.18u)' nrd='0.18u / W' nrs='0.18u / W'
+ sa=0 sb=0 sd=0 m=1
XM58 VDD VDD VDD VDD pfet_03v3 L=0.28u W=24u nf=1 ad='int((nf+1)/2) * W/nf * 0.18u' as='int((nf+2)/2) * W/nf * 0.18u'
+ pd='2*int((nf+1)/2) * (W/nf + 0.18u)' ps='2*int((nf+2)/2) * (W/nf + 0.18u)' nrd='0.18u / W' nrs='0.18u / W'
+ sa=0 sb=0 sd=0 m=1
XM59 VDD VDD VDD VDD pfet_03v3 L=0.28u W=24u nf=1 ad='int((nf+1)/2) * W/nf * 0.18u' as='int((nf+2)/2) * W/nf * 0.18u'
+ pd='2*int((nf+1)/2) * (W/nf + 0.18u)' ps='2*int((nf+2)/2) * (W/nf + 0.18u)' nrd='0.18u / W' nrs='0.18u / W'
+ sa=0 sb=0 sd=0 m=1
XM60 VDD VDD VDD VDD pfet_03v3 L=0.28u W=24u nf=1 ad='int((nf+1)/2) * W/nf * 0.18u' as='int((nf+2)/2) * W/nf * 0.18u'
+ pd='2*int((nf+1)/2) * (W/nf + 0.18u)' ps='2*int((nf+2)/2) * (W/nf + 0.18u)' nrd='0.18u / W' nrs='0.18u / W'
+ sa=0 sb=0 sd=0 m=1
XM61 VDD VDD VDD VDD pfet_03v3 L=0.28u W=24u nf=1 ad='int((nf+1)/2) * W/nf * 0.18u' as='int((nf+2)/2) * W/nf * 0.18u'
+ pd='2*int((nf+1)/2) * (W/nf + 0.18u)' ps='2*int((nf+2)/2) * (W/nf + 0.18u)' nrd='0.18u / W' nrs='0.18u / W'
+ sa=0 sb=0 sd=0 m=1
XM62 VDD VDD VDD VDD pfet_03v3 L=0.28u W=32u nf=1 ad='int((nf+1)/2) * W/nf * 0.18u' as='int((nf+2)/2) * W/nf * 0.18u'
+ pd='2*int((nf+1)/2) * (W/nf + 0.18u)' ps='2*int((nf+2)/2) * (W/nf + 0.18u)' nrd='0.18u / W' nrs='0.18u / W'
+ sa=0 sb=0 sd=0 m=1
XM74 VDD VDD VDD VDD pfet_03v3 L=0.28u W=1u nf=1 ad='int((nf+1)/2) * W/nf * 0.18u' as='int((nf+2)/2) * W/nf * 0.18u'
+ pd='2*int((nf+1)/2) * (W/nf + 0.18u)' ps='2*int((nf+2)/2) * (W/nf + 0.18u)' nrd='0.18u / W' nrs='0.18u / W'
+ sa=0 sb=0 sd=0 m=1
XM84 VDD VDD VDD VDD pfet_03v3 L=0.28u W=30u nf=1 ad='int((nf+1)/2) * W/nf * 0.18u' as='int((nf+2)/2) * W/nf * 0.18u'
+ pd='2*int((nf+1)/2) * (W/nf + 0.18u)' ps='2*int((nf+2)/2) * (W/nf + 0.18u)' nrd='0.18u / W' nrs='0.18u / W'
+ sa=0 sb=0 sd=0 m=1
.ends

.GLOBAL GND
.end
